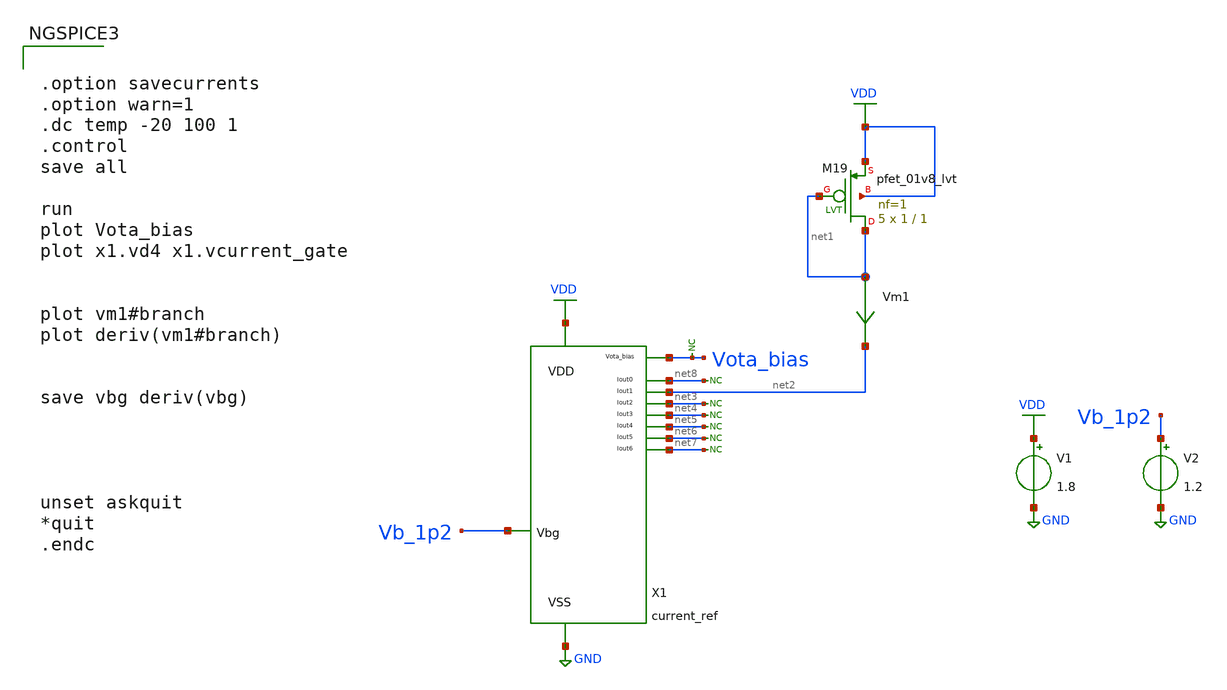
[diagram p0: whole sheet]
** sch_path: xschem/current_reference/tb_current_ref_pvt_lvs.sch
**.subckt tb_current_ref_pvt_lvs
V1 VDD GND 1.8
XM19 net1 net1 VDD VDD sky130_fd_pr__pfet_01v8_lvt L=1 W=1 nf=1 ad='int((nf+1)/2) * W/nf * 0.29' as='int((nf+2)/2) * W/nf * 0.29'
+ pd='2*int((nf+1)/2) * (W/nf + 0.29)' ps='2*int((nf+2)/2) * (W/nf + 0.29)' nrd='0.29 / W' nrs='0.29 / W'
+ sa=0 sb=0 sd=0 mult=5 m=5
Vm1 net1 net2 0
.save i(vm1)
* noconn #net3
* noconn #net4
* noconn #net5
* noconn #net6
* noconn #net7
* noconn #net8
X1 Vb_1p2 VDD GND net8 net2 net3 net4 net5 net6 net7 Vota_bias current_ref
V2 Vb_1p2 GND 1.2
* noconn Vota_bias
**** begin user architecture code

** opencircuitdesign pdks install
.lib $::SKYWATER_MODELS/sky130.lib.spice tt




.option savecurrents
.option warn=1
.dc temp -20 100 1
.control
save all

run
plot Vota_bias
plot x1.vd4 x1.vcurrent_gate


plot vm1#branch
plot deriv(vm1#branch)


save vbg deriv(vbg)




unset askquit
*quit
.endc


**** end user architecture code
**.ends
.GLOBAL VDD
.GLOBAL GND
.end
